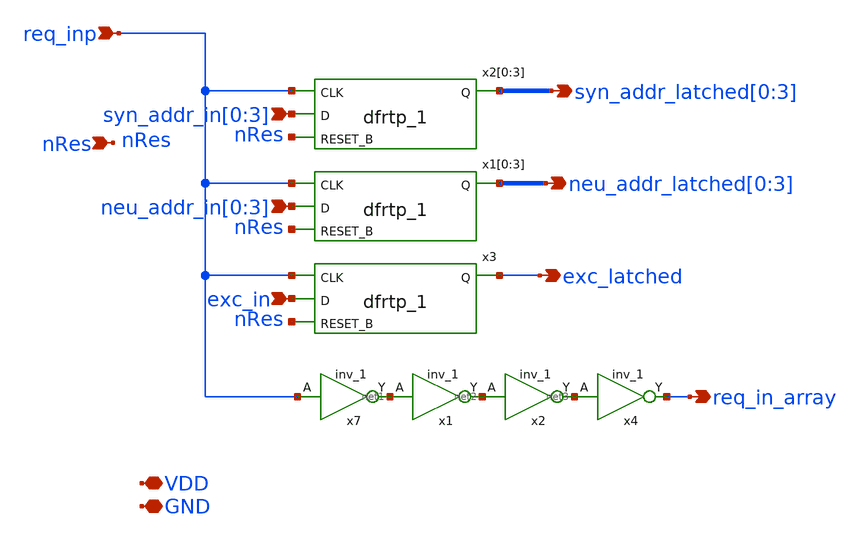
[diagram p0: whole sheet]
** sch_path: design/xschem/inputs_latch_16neu.sch
**.subckt inputs_latch_16neu neu_addr_in[0],neu_addr_in[1],neu_addr_in[2],neu_addr_in[3] req_inp
*+ syn_addr_in[0],syn_addr_in[1],syn_addr_in[2],syn_addr_in[3] exc_in nRes syn_addr_latched[0],syn_addr_latched[1],syn_addr_latched[2],syn_addr_latched[3]
*+ neu_addr_latched[0],neu_addr_latched[1],neu_addr_latched[2],neu_addr_latched[3] exc_latched req_in_array VDD GND
*.ipin neu_addr_in[0],neu_addr_in[1],neu_addr_in[2],neu_addr_in[3]
*.ipin req_inp
*.ipin syn_addr_in[0],syn_addr_in[1],syn_addr_in[2],syn_addr_in[3]
*.ipin exc_in
*.ipin nRes
*.opin syn_addr_latched[0],syn_addr_latched[1],syn_addr_latched[2],syn_addr_latched[3]
*.opin neu_addr_latched[0],neu_addr_latched[1],neu_addr_latched[2],neu_addr_latched[3]
*.opin exc_latched
*.opin req_in_array
*.iopin VDD
*.iopin GND
x2[0] req_inp syn_addr_in[0] nRes GND GND VDD VDD syn_addr_latched[0] sky130_fd_sc_hd__dfrtp_1
x2[1] req_inp syn_addr_in[1] nRes GND GND VDD VDD syn_addr_latched[1] sky130_fd_sc_hd__dfrtp_1
x2[2] req_inp syn_addr_in[2] nRes GND GND VDD VDD syn_addr_latched[2] sky130_fd_sc_hd__dfrtp_1
x2[3] req_inp syn_addr_in[3] nRes GND GND VDD VDD syn_addr_latched[3] sky130_fd_sc_hd__dfrtp_1
x1[0] req_inp neu_addr_in[0] nRes GND GND VDD VDD neu_addr_latched[0] sky130_fd_sc_hd__dfrtp_1
x1[1] req_inp neu_addr_in[1] nRes GND GND VDD VDD neu_addr_latched[1] sky130_fd_sc_hd__dfrtp_1
x1[2] req_inp neu_addr_in[2] nRes GND GND VDD VDD neu_addr_latched[2] sky130_fd_sc_hd__dfrtp_1
x1[3] req_inp neu_addr_in[3] nRes GND GND VDD VDD neu_addr_latched[3] sky130_fd_sc_hd__dfrtp_1
x3 req_inp exc_in nRes GND GND VDD VDD exc_latched sky130_fd_sc_hd__dfrtp_1
x7 req_inp GND GND VDD VDD net1 sky130_fd_sc_hd__inv_1
x1 net1 GND GND VDD VDD net2 sky130_fd_sc_hd__inv_1
x2 net2 GND GND VDD VDD net3 sky130_fd_sc_hd__inv_1
x4 net3 GND GND VDD VDD req_in_array sky130_fd_sc_hd__inv_1
**.ends
.end
